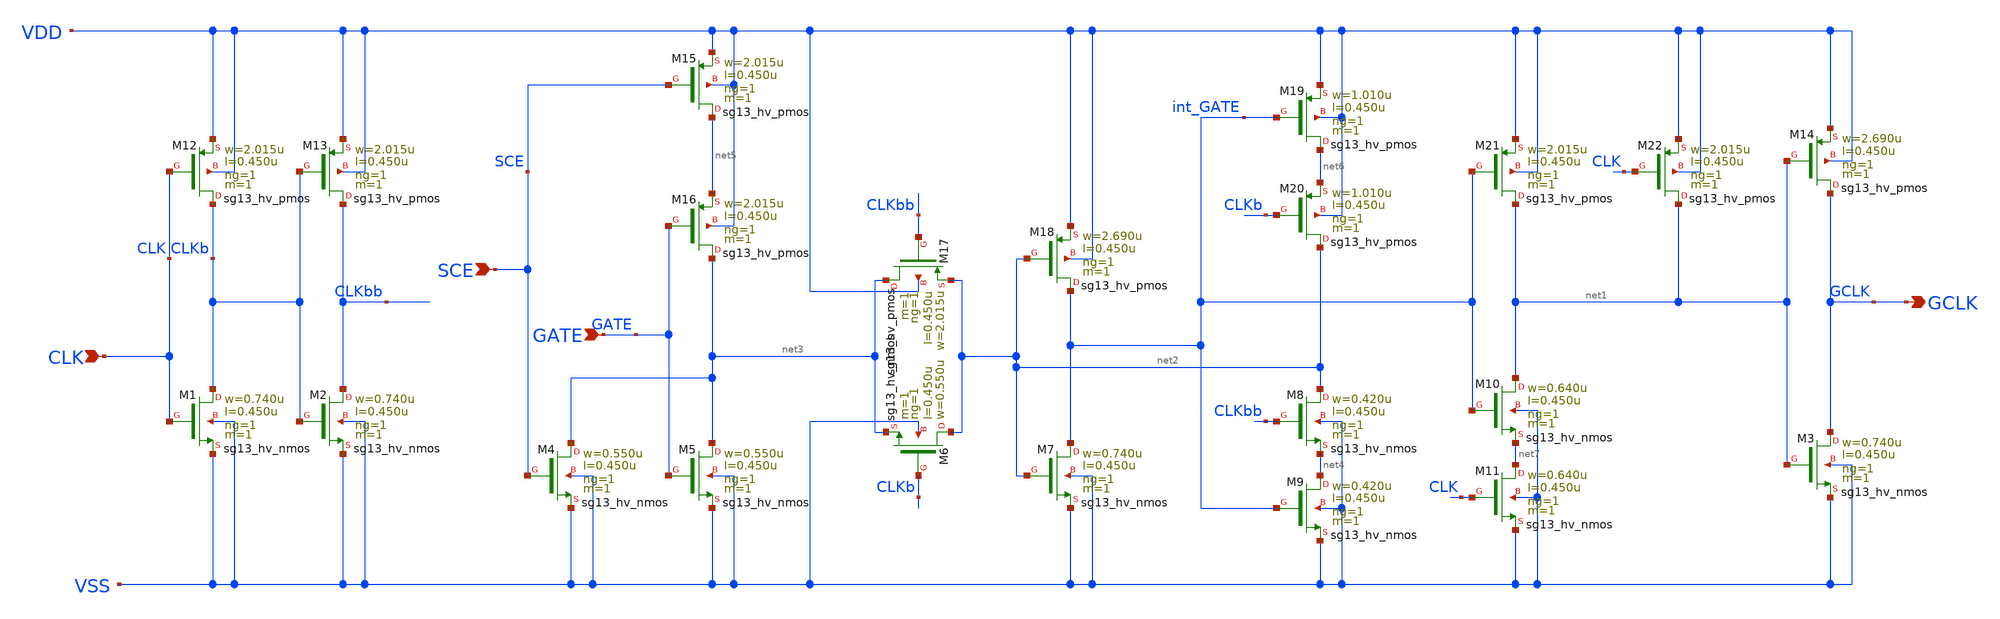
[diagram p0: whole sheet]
** sch_path: ihp-sg13g2/libs.ref/sg13g2_stdcell_hv/sch/xschem/sg13g2_hv_slgcp_1.sch
* Copyright 2023 IHP PDK Authors
* Licensed under the Apache License, Version 2.0 (the "License");
* you may not use this file except in compliance with the License.
* You may obtain a copy of the License at
* https://www.apache.org/licenses/LICENSE-2.0
* Unless required by applicable law or agreed to in writing, software
* distributed under the License is distributed on an "AS IS" BASIS,
* WITHOUT WARRANTIES OR CONDITIONS OF ANY KIND, either express or implied.
* See the License for the specific language governing permissions and
* limitations under the License.
**.subckt sg13g2_hv_slgcp_1 GCLK SCE GATE CLK
*.opin GCLK
*.ipin SCE
*.ipin GATE
*.ipin CLK
XM1 CLKb CLK VSS VSS sg13_hv_nmos w=0.740u l=0.450u ng=1 m=1 mm_ok=1
XM2 CLKbb CLKb VSS VSS sg13_hv_nmos w=0.740u l=0.450u ng=1 m=1 mm_ok=1
XM3 GCLK net1 VSS VSS sg13_hv_nmos w=0.740u l=0.450u ng=1 m=1 mm_ok=1
XM4 net3 SCE VSS VSS sg13_hv_nmos w=0.550u l=0.450u ng=1 m=1 mm_ok=1
XM5 net3 GATE VSS VSS sg13_hv_nmos w=0.550u l=0.450u ng=1 m=1 mm_ok=1
XM6 net2 CLKb net3 VSS sg13_hv_nmos w=0.550u l=0.450u ng=1 m=1 mm_ok=1
XM7 int_GATE net2 VSS VSS sg13_hv_nmos w=0.740u l=0.450u ng=1 m=1 mm_ok=1
XM8 net2 CLKbb net4 VSS sg13_hv_nmos w=0.420u l=0.450u ng=1 m=1 mm_ok=1
XM9 net4 int_GATE VSS VSS sg13_hv_nmos w=0.420u l=0.450u ng=1 m=1 mm_ok=1
XM10 net1 int_GATE net7 VSS sg13_hv_nmos w=0.640u l=0.450u ng=1 m=1 mm_ok=1
XM11 net7 CLK VSS VSS sg13_hv_nmos w=0.640u l=0.450u ng=1 m=1 mm_ok=1
XM12 CLKb CLK VDD VDD sg13_hv_pmos w=2.015u l=0.450u ng=1 m=1 mm_ok=1
XM13 CLKbb CLKb VDD VDD sg13_hv_pmos w=2.015u l=0.450u ng=1 m=1 mm_ok=1
XM14 GCLK net1 VDD VDD sg13_hv_pmos w=2.690u l=0.450u ng=1 m=1 mm_ok=1
XM15 net5 SCE VDD VDD sg13_hv_pmos w=2.015u l=0.450u ng=1 m=1 mm_ok=1
XM16 net3 GATE net5 VDD sg13_hv_pmos w=2.015u l=0.450u ng=1 m=1 mm_ok=1
XM17 net3 CLKbb net2 VDD sg13_hv_pmos w=2.015u l=0.450u ng=1 m=1 mm_ok=1
XM18 int_GATE net2 VDD VDD sg13_hv_pmos w=2.690u l=0.450u ng=1 m=1 mm_ok=1
XM19 net6 int_GATE VDD VDD sg13_hv_pmos w=1.010u l=0.450u ng=1 m=1 mm_ok=1
XM20 net2 CLKb net6 VDD sg13_hv_pmos w=1.010u l=0.450u ng=1 m=1 mm_ok=1
XM21 net1 int_GATE VDD VDD sg13_hv_pmos w=2.015u l=0.450u ng=1 m=1 mm_ok=1
XM22 net1 CLK VDD VDD sg13_hv_pmos w=2.015u l=0.450u ng=1 m=1 mm_ok=1
**.ends
.end
